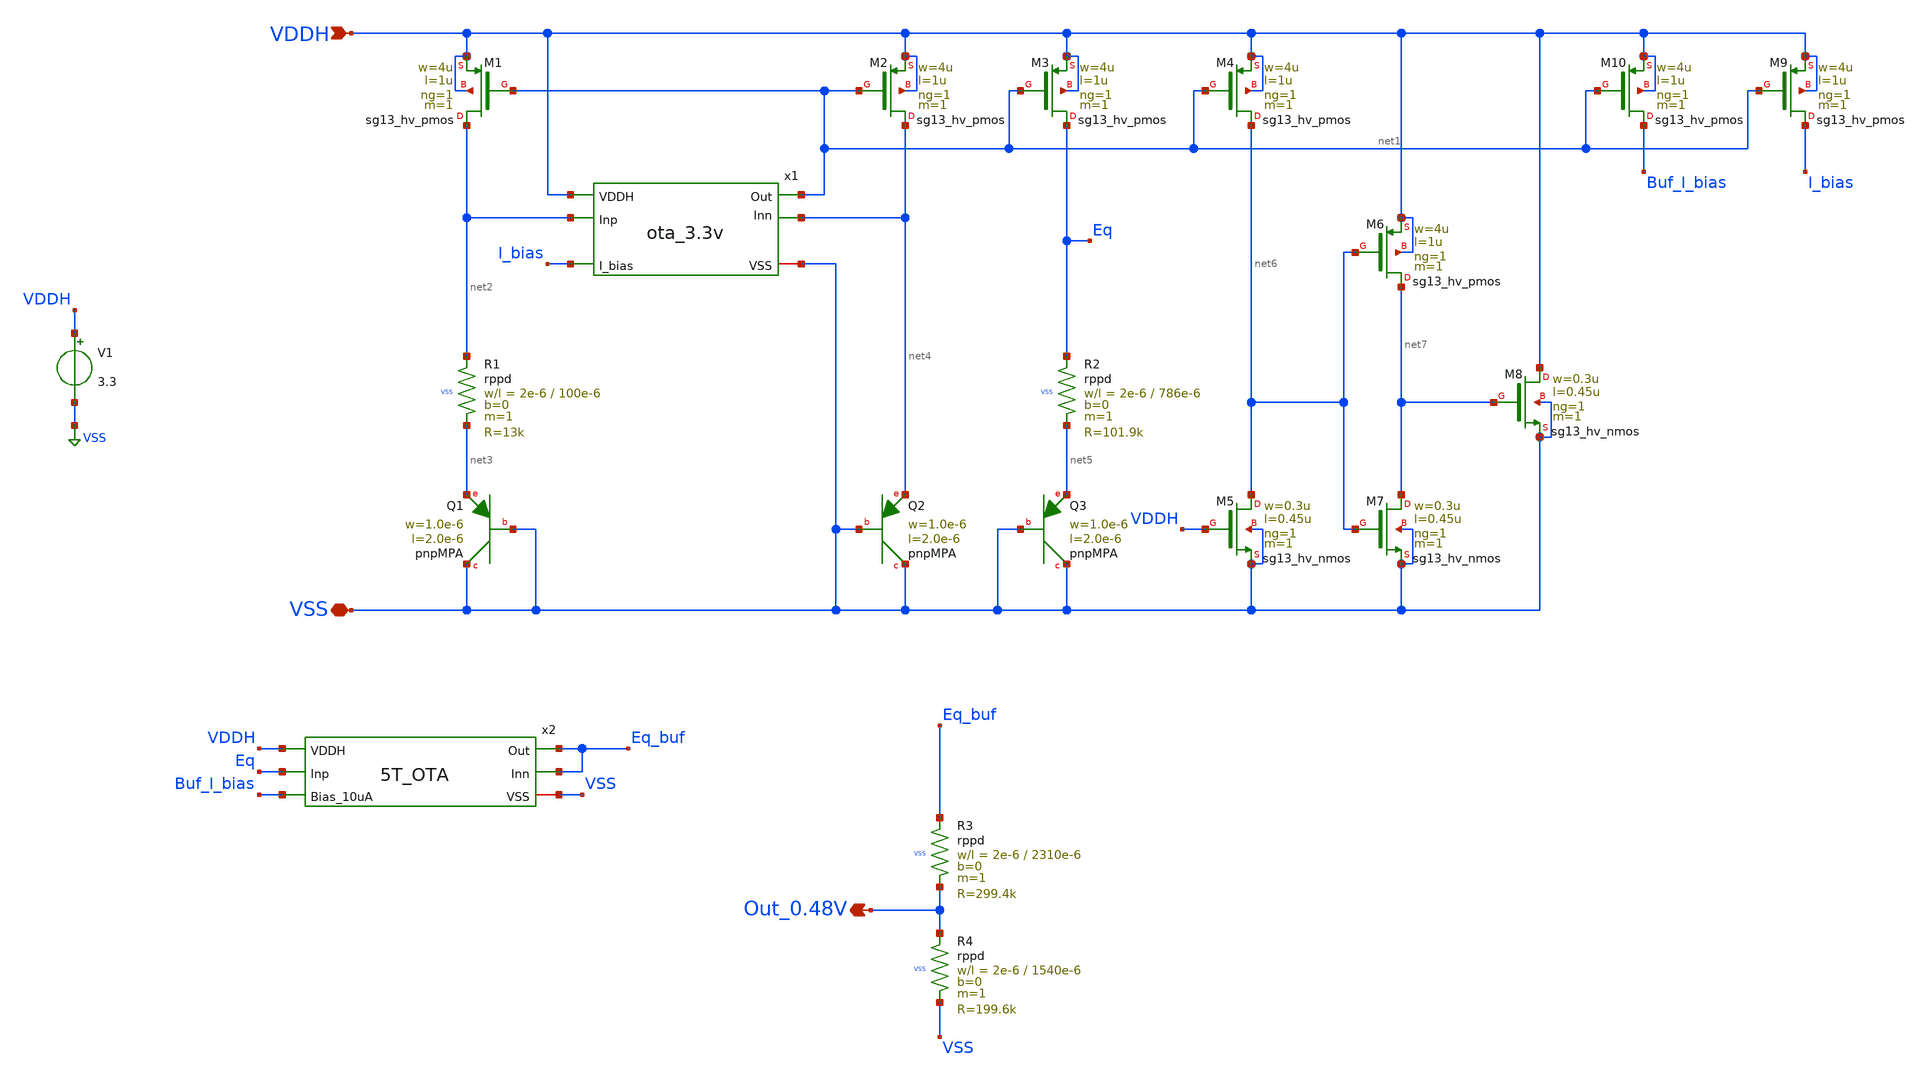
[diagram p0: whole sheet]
** sch_path: sar_adc/xschem/blocks/bandgap/0.48v_bandgap_tb.sch
**.subckt 0.48v_bandgap_tb VDDH VSS Out_0.48V
*.ipin VDDH
*.iopin VSS
*.opin Out_0.48V
XM1 net2 net1 VDDH VDDH sg13_hv_pmos w=4u l=1u ng=1 m=1 mm_ok=1
x1 VDDH net2 net4 net1 I_bias VSS ota_3.3v
XM2 net4 net1 VDDH VDDH sg13_hv_pmos w=4u l=1u ng=1 m=1 mm_ok=1
XR1 net2 net3 VSS rppd w=2e-6 l=100e-6 m=1 b=0 mm_ok=1
XQ1 VSS VSS net3 pnpMPA a=2p p=6u m=8
XQ2 VSS VSS net4 pnpMPA a=2p p=6u m=1
V1 VDDH VSS 3.3
XM3 Eq net1 VDDH VDDH sg13_hv_pmos w=4u l=1u ng=1 m=1 mm_ok=1
XQ3 VSS VSS net5 pnpMPA a=2p p=6u m=1
XR2 Eq net5 VSS rppd w=2e-6 l=786e-6 m=1 b=0 mm_ok=1
XM4 net6 net1 VDDH VDDH sg13_hv_pmos w=4u l=1u ng=1 m=1 mm_ok=1
XM5 net6 VDDH VSS VSS sg13_hv_nmos w=0.3u l=0.45u ng=1 m=1 mm_ok=1
XM6 net7 net6 VDDH VDDH sg13_hv_pmos w=4u l=1u ng=1 m=1 mm_ok=1
XM7 net7 net6 VSS VSS sg13_hv_nmos w=0.3u l=0.45u ng=1 m=1 mm_ok=1
XM8 VDDH net7 VSS VSS sg13_hv_nmos w=0.3u l=0.45u ng=1 m=1 mm_ok=1
XM9 I_bias net1 VDDH VDDH sg13_hv_pmos w=4u l=1u ng=1 m=1 mm_ok=1
x2 VDDH Eq_buf Eq_buf Eq Buf_I_bias VSS 5T_OTA
XR3 Eq_buf Out_0.48V VSS rppd w=2e-6 l=2310e-6 m=1 b=0 mm_ok=1
XR4 Out_0.48V VSS VSS rppd w=2e-6 l=1540e-6 m=1 b=0 mm_ok=1
XM10 Buf_I_bias net1 VDDH VDDH sg13_hv_pmos w=4u l=1u ng=1 m=1 mm_ok=1
**** begin user architecture code

.lib $::SG13G2_MODELS/cornerMOShv.lib mos_tt
.lib $::SG13G2_MODELS/cornerRES.lib res_typ
.lib $::SG13G2_MODELS/cornerCAP.lib cap_typ
.lib $::SG13G2_MODELS/cornerHBT.lib hbt_typ



.control
 save all

set temp=27
op
echo === OP node voltages ===
print net1 net2 net3 net4 inn eq
print n.xr1.nr1#i1 n.xr1.nr1#i2
print n.xm1.nsg13_hv_pmos#di
print n.xm3.nsg13_hv_pmos#di

dc temp -40 125 1

* Correct nodes after netlist analysis:
* Inn  = Q2 emitter = Vbe (CTAT reference)
* net2 = top of XR1 = OTA.Inp (tracks Inn when loop closed)
* net3 = bottom of XR1 = Q1 emitter
* ΔVbe = net2 - net3

let vbe   = dc1.inn
let vdvbe = dc1.net2 - dc1.net3
let veq   = dc1.eq
let vnet4 = dc1.net4

* Vbe CTAT stats
let vbe_max = vecmax(vbe)
let vbe_min = vecmin(vbe)
let vbe_nom = mean(vbe)
let tc_vbe  = ((vbe_max - vbe_min) / vbe_nom) * 1e6 / 165

* ΔVbe PTAT stats
let vr_max = vecmax(vdvbe)
let vr_min = vecmin(vdvbe)
let vr_nom = mean(vdvbe)
let tc_vr  = ((vr_max - vr_min) / vr_nom) * 1e6 / 165

* PTAT current
let i_ptat    = vdvbe / 13e3
let i_ptat_ua = i_ptat * 1e6

* CATA output
let veq_max = vecmax(veq)
let veq_min = vecmin(veq)
let veq_nom = mean(veq)
let tc_eq   = ((veq_max - veq_min) / veq_nom) * 1e6 / 165

echo === Vbe CTAT (Inn) ===
print vbe_max vbe_min vbe_nom tc_vbe

echo === Delta_Vbe PTAT (net2-net3) ===
print vr_max vr_min vr_nom tc_vr

echo === I_PTAT uA ===
print vecmax(i_ptat_ua) vecmin(i_ptat_ua) mean(i_ptat_ua)

echo === Eq bandgap output ===
print veq_max veq_min veq_nom tc_eq

echo === net4 Q3 emitter ===
print vecmax(vnet4) vecmin(vnet4) mean(vnet4)

plot dc1.inn title 'Vbe vs T (CTAT)'
plot dc1.net2 - dc1.net3 title 'Delta_Vbe vs T (PTAT)'
plot dc1.eq title 'Eq bandgap output vs T'
plot i_ptat_ua title 'I_PTAT uA vs T'

wrdata /tmp/bg_inn.txt dc1.inn
wrdata /tmp/bg_eq.txt dc1.eq

echo === Eq bandgap output ===
print veq_max veq_min veq_nom tc_eq

* Better TC calculation — use max deviation from nominal
let veq_center = (veq_max + veq_min) / 2
let tc_eq_pp = (veq_max - veq_min) / veq_center * 1e6 / 165
print tc_eq_pp


print v(Eq_buf)
print v(Out_0.48V)
print n.xr3.nr1#i1


.endc


**** end user architecture code
**.ends

* expanding   symbol:  Projektai/SG13G2/SAR_ADC/ota_3.3v.sym # of pins=6
** sym_path: sar_adc/xschem/blocks/cascode_ota/ota_3.3v.sym
** sch_path: sar_adc/xschem/blocks/cascode_ota/ota_3.3v.sch
.subckt ota_3.3v VDDH Inp Inn Out I_bias VSS
*.ipin VDDH
*.iopin VSS
*.ipin I_bias
*.opin Out
*.ipin Inp
*.ipin Inn
XM2 net1 net1 VDDH VDDH sg13_hv_pmos w=10u l=1u ng=1 m=1 mm_ok=1
XM3 net1 I_bias VSS VSS sg13_hv_nmos w=3u l=3u ng=1 m=1 mm_ok=1
XM1 I_bias I_bias VSS VSS sg13_hv_nmos w=3u l=3u ng=1 m=1 mm_ok=1
XM11 net8 I_bias VSS VSS sg13_hv_nmos w=3u l=3u ng=1 m=1 mm_ok=1
XM13 net5 Inp net2 VDDH sg13_hv_pmos w=8u l=1u ng=2 m=1 mm_ok=1
XM14 net6 Inn net2 VDDH sg13_hv_pmos w=8u l=1u ng=2 m=1 mm_ok=1
XM15 net7 net4 VDDH VDDH sg13_hv_pmos w=10u l=1u ng=1 m=1 mm_ok=1
XM20 net3 net4 VDDH VDDH sg13_hv_pmos w=10u l=1u ng=1 m=1 mm_ok=1
XM17 net4 v_net3 net7 VDDH sg13_hv_pmos w=10u l=1u ng=1 m=1 mm_ok=1
XM18 net4 v_net2 net5 VSS sg13_hv_nmos w=10u l=1u ng=1 m=1 mm_ok=1
XM19 net5 v_net1 VSS VSS sg13_hv_nmos w=9u l=1u ng=1 m=1 mm_ok=1
XM22 Out v_net2 net6 VSS sg13_hv_nmos w=10u l=1u ng=1 m=1 mm_ok=1
XM23 net6 v_net1 VSS VSS sg13_hv_nmos w=9u l=1u ng=1 m=1 mm_ok=1
XM12 net2 net8 VDDH VDDH sg13_hv_pmos w=10u l=1u ng=1 m=1 mm_ok=1
XM10 net8 net8 VDDH VDDH sg13_hv_pmos w=10u l=1u ng=1 m=1 mm_ok=1
XM6 v_net1 v_net1 VSS VSS sg13_hv_nmos w=8u l=1u ng=1 m=1 mm_ok=1
XM4 v_net2 net1 VDDH VDDH sg13_hv_pmos w=10u l=1u ng=1 m=1 mm_ok=1
XM5 v_net2 v_net2 v_net1 VSS sg13_hv_nmos w=10u l=1u ng=2 m=1 mm_ok=1
XM7 net9 net9 VDDH VDDH sg13_hv_pmos w=10u l=1u ng=1 m=1 mm_ok=1
XM9 v_net3 I_bias VSS VSS sg13_hv_nmos w=1.9u l=3u ng=1 m=1 mm_ok=1
XM8 v_net3 v_net3 net9 VDDH sg13_hv_pmos w=10u l=1u ng=1 m=1 mm_ok=1
XM21 Out v_net3 net3 VDDH sg13_hv_pmos w=10u l=1u ng=1 m=1 mm_ok=1
.ends


* expanding   symbol:  Projektai/SG13G2/SAR_ADC/5T_OTA.sym # of pins=6
** sym_path: sar_adc/xschem/blocks/5t_ota/5T_OTA.sym
** sch_path: sar_adc/xschem/blocks/5t_ota/5T_OTA.sch
.subckt 5T_OTA VDDH Out Inn Inp Bias_10uA VSS
*.ipin VDDH
*.opin Out
*.iopin VSS
*.ipin Bias_10uA
*.ipin Inp
*.ipin Inn
XM1 net1 net1 VDDH VDDH sg13_hv_pmos w=5u l=6u ng=1 m=4 mm_ok=1
XM2 Out net1 VDDH VDDH sg13_hv_pmos w=5u l=6u ng=1 m=4 mm_ok=1
XM3 net1 Inp net2 VSS sg13_hv_nmos w=10u l=2u ng=1 m=4 mm_ok=1
XM4 Out Inn net2 VSS sg13_hv_nmos w=10u l=2u ng=1 m=4 mm_ok=1
XM5 net2 Bias_10uA VSS VSS sg13_hv_nmos w=5u l=2u ng=1 m=12 mm_ok=1
XM6 Bias_10uA Bias_10uA VSS VSS sg13_hv_nmos w=5u l=2u ng=1 m=2 mm_ok=1
.ends

.GLOBAL VSS
.end
